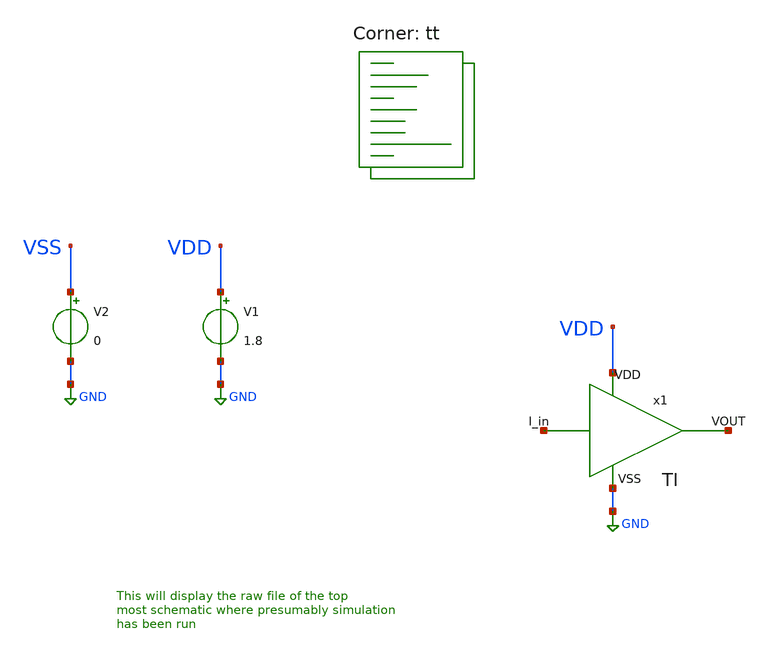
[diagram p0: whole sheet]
** sch_path: my_ip/sky130A/TIA_1_8_V2/testbenches/tb.sch
**.subckt tb
V1 VDD GND 1.8
V2 VSS GND 0
x1 VDD GND net1 net2 TI
**** begin user architecture code
.lib $::SKYWATER_MODELS/sky130.lib.spice tt
**** end user architecture code
**.ends

* expanding   symbol:  /home/gim/Desktop/OSAD/my_ip/sky130A/TIA_1_8_V2/TI.sym # of pins=4
** sym_path: my_ip/sky130A/TIA_1_8_V2/TI.sym
** sch_path: my_ip/sky130A/TIA_1_8_V2/TI.sch
.subckt TI VDD VSS I_in VOUT
*.iopin VDD
*.iopin VSS
*.iopin I_in
*.iopin VOUT
XM1 net1 net1 VDD VDD sky130_fd_pr__pfet_01v8_lvt L=1 W='10 * 2 ' nf=2 ad='int((2 + 1)/2) * 10 / 2 * 0.29'
+ as='int((2 + 2)/2) * 10 / 2 * 0.29' pd='2*int((2 + 1)/2) * (10 / 2 + 0.29)' ps='2*int((2 + 2)/2) * (10 / 2 + 0.29)'
+ nrd='0.29 / 10 ' nrs='0.29 / 10 ' sa=0 sb=0 sd=0 mult=4 m=4
XM2 net2 net1 VDD VDD sky130_fd_pr__pfet_01v8_lvt L=1 W='10 * 2 ' nf=2 ad='int((2 + 1)/2) * 10 / 2 * 0.29'
+ as='int((2 + 2)/2) * 10 / 2 * 0.29' pd='2*int((2 + 1)/2) * (10 / 2 + 0.29)' ps='2*int((2 + 2)/2) * (10 / 2 + 0.29)'
+ nrd='0.29 / 10 ' nrs='0.29 / 10 ' sa=0 sb=0 sd=0 mult=4 m=4
XM3 net2 net2 net3 VSS sky130_fd_pr__nfet_01v8_lvt L=0.6 W='5 * 2 ' nf=2 ad='int((2 + 1)/2) * 5 / 2 * 0.29'
+ as='int((2 + 2)/2) * 5 / 2 * 0.29' pd='2*int((2 + 1)/2) * (5 / 2 + 0.29)' ps='2*int((2 + 2)/2) * (5 / 2 + 0.29)'
+ nrd='0.29 / 5 ' nrs='0.29 / 5 ' sa=0 sb=0 sd=0 mult=4 m=4
XM4 net1 net2 net4 VSS sky130_fd_pr__nfet_01v8_lvt L=0.6 W='5 * 2 ' nf=2 ad='int((2 + 1)/2) * 5 / 2 * 0.29'
+ as='int((2 + 2)/2) * 5 / 2 * 0.29' pd='2*int((2 + 1)/2) * (5 / 2 + 0.29)' ps='2*int((2 + 2)/2) * (5 / 2 + 0.29)'
+ nrd='0.29 / 5 ' nrs='0.29 / 5 ' sa=0 sb=0 sd=0 mult=4 m=4
XM5 net3 net3 net5 net7 sky130_fd_pr__nfet_01v8_lvt L=0.6 W='5 * 2 ' nf=2 ad='int((2 + 1)/2) * 5 / 2 * 0.29'
+ as='int((2 + 2)/2) * 5 / 2 * 0.29' pd='2*int((2 + 1)/2) * (5 / 2 + 0.29)' ps='2*int((2 + 2)/2) * (5 / 2 + 0.29)'
+ nrd='0.29 / 5 ' nrs='0.29 / 5 ' sa=0 sb=0 sd=0 mult=4 m=4
XM6 net4 net3 net6 net8 sky130_fd_pr__nfet_01v8_lvt L=0.6 W='5 * 2 ' nf=2 ad='int((2 + 1)/2) * 5 / 2 * 0.29'
+ as='int((2 + 2)/2) * 5 / 2 * 0.29' pd='2*int((2 + 1)/2) * (5 / 2 + 0.29)' ps='2*int((2 + 2)/2) * (5 / 2 + 0.29)'
+ nrd='0.29 / 5 ' nrs='0.29 / 5 ' sa=0 sb=0 sd=0 mult=4 m=4
.ends

.GLOBAL GND
**** begin user architecture code


* ngspice commands
.options savecurrents
.TEMP 27
.control
save all
save @m.x1.xm1.msky130_fd_pr__pfet_01v8_lvt[gm]
save @m.x1.xm1.msky130_fd_pr__pfet_01v8_lvt[vth]
save @m.x1.xm1.msky130_fd_pr__pfet_01v8_lvt[gds]
save @m.x1.xm1.msky130_fd_pr__pfet_01v8_lvt[gmbs]
save @m.x1.xm1.msky130_fd_pr__pfet_01v8_lvt[vds]
save @m.x1.xm1.msky130_fd_pr__pfet_01v8_lvt[vgs]

save @m.x1.xm2.msky130_fd_pr__pfet_01v8_lvt[gm]
save @m.x1.xm2.msky130_fd_pr__pfet_01v8_lvt[vth]
save @m.x1.xm2.msky130_fd_pr__pfet_01v8_lvt[gds]
save @m.x1.xm2.msky130_fd_pr__pfet_01v8_lvt[gmbs]
save @m.x1.xm2.msky130_fd_pr__pfet_01v8_lvt[vds]
save @m.x1.xm2.msky130_fd_pr__pfet_01v8_lvt[vgs]

save @m.x1.xm3.msky130_fd_pr__nfet_01v8_lvt[gm]
save @m.x1.xm3.msky130_fd_pr__nfet_01v8_lvt[vth]
save @m.x1.xm3.msky130_fd_pr__nfet_01v8_lvt[gds]
save @m.x1.xm3.msky130_fd_pr__nfet_01v8_lvt[gmbs]
save @m.x1.xm3.msky130_fd_pr__nfet_01v8_lvt[vds]
save @m.x1.xm3.msky130_fd_pr__nfet_01v8_lvt[vgs]

save @m.x1.xm4.msky130_fd_pr__nfet_01v8_lvt[gm]
save @m.x1.xm4.msky130_fd_pr__nfet_01v8_lvt[vth]
save @m.x1.xm4.msky130_fd_pr__nfet_01v8_lvt[gds]
save @m.x1.xm4.msky130_fd_pr__nfet_01v8_lvt[gmbs]
save @m.x1.xm4.msky130_fd_pr__nfet_01v8_lvt[vds]
save @m.x1.xm4.msky130_fd_pr__nfet_01v8_lvt[vgs]


op
write tb.raw

.endc



**** end user architecture code
.end
